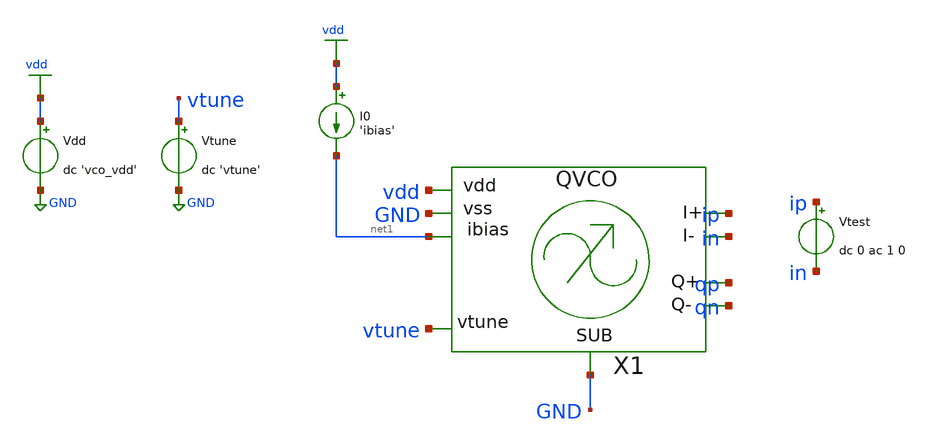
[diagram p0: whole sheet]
** sch_path: tb/vco/tb_loop_gain.sch
**.subckt tb_loop_gain
Vdd vdd GND dc 'vco_vdd'
Vtune vtune GND dc 'vtune'
X1 vdd GND vtune ip in qp qn GND net1 vco m=1
I0 vdd net1 'ibias'
Vtest ip in dc 0 ac 1 0
**** begin user architecture code


.include 'models_dir'/design.spice
.lib 'models_dir'/sm141064.spice 'mos_corner'
.lib 'models_dir'/sm141064.spice moscap_'mos_corner'
.option TEMP='temperature'
.option warn=1
.option rshunt=1e12
.control
save all
ac dec 100 1meg 20g
let y11 = -i(vtest) / (v(ip) - v(in))
let y11_re = real(y11)
let y11_im = imag(y11)
set wr_singlescale
wrdata 'simpath'/'filename'_'N'.data y11_re y11_im
quit
.endc


**** end user architecture code
**.ends
.GLOBAL GND
.GLOBAL vdd
.end
